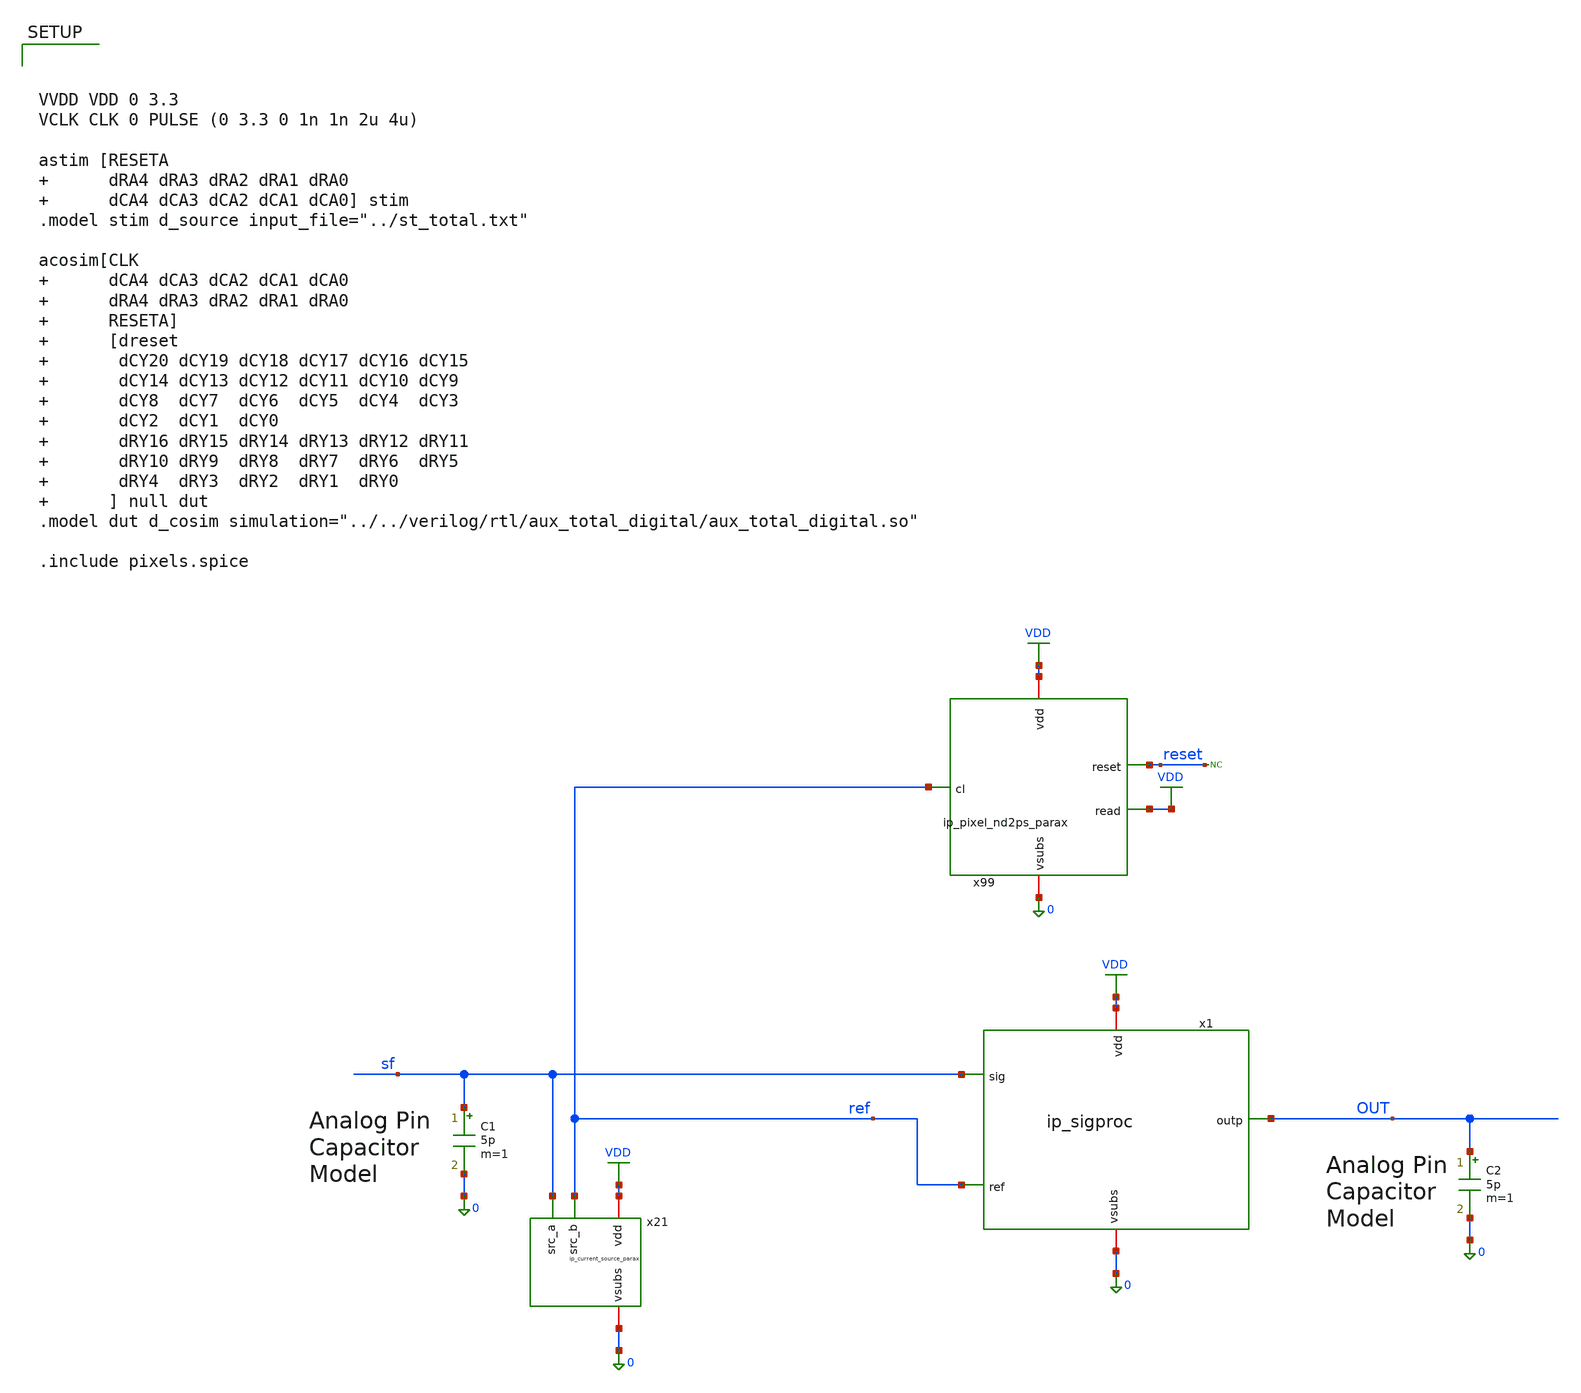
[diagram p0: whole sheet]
** sch_path: xschem/tb_total_tran.sch
**.subckt tb_total_tran
x21 VDD sf 0 ref ip_current_source_parax
x99 VDD reset VDD 0 ref ip_pixel_nd2ps_parax
C1 sf 0 5p m=1
C2 OUT 0 5p m=1
* noconn reset
x1 VDD OUT sf ref 0 ip_sigproc
**** begin user architecture code

.include $::180MCU_MODELS/design.ngspice
.lib $::180MCU_MODELS/sm141064.ngspice typical
.lib $::180MCU_MODELS/sm141064.ngspice res_typical
.lib $::180MCU_MODELS/sm141064.ngspice moscap_typical
.lib $::180MCU_MODELS/sm141064.ngspice diode_typical




.option klu
.option reltol=0.075
.option abstol=200u
.save none

.save V(nRA0) V(nRA1) V(nRA2) V(nRA3) V(nRA4)
.save V(nCA0) V(nCA1) V(nCA2) V(nCA3) V(nCA4)

.save V(ncy0) V(ncy1) V(ncy2) V(ncy3) V(ncy4) V(ncy5) V(ncy6) V(ncy7) V(ncy8)
.save V(ncy9) V(ncy10) V(ncy11) V(ncy12) V(ncy13) V(ncy14) V(ncy15) V(ncy16)
.save V(ncy17) V(ncy18) V(ncy19) V(ncy20)

.save V(nry0) V(nry1) V(nry2) V(nry3) V(nry4) V(nry5) V(nry6) V(nry7) V(nry8)
.save V(nry9) V(nry10) V(nry11) V(nry12) V(nry13) V(nry14) V(nry15) V(nry16)

.save V(reset) V(clk)
.save V(out) V(sf) V(ref) V(amp)
.control
	reset
	tran 1u 9m
	write tb_total_tran.raw
	quit
.endc






VVDD VDD 0 3.3
VCLK CLK 0 PULSE (0 3.3 0 1n 1n 2u 4u)

astim [RESETA        dRA4 dRA3 dRA2 dRA1 dRA0        dCA4 dCA3 dCA2 dCA1 dCA0] stim
.model stim d_source input_file="../st_total.txt"

acosim[CLK        dCA4 dCA3 dCA2 dCA1 dCA0        dRA4 dRA3 dRA2 dRA1 dRA0        RESETA]
+        [dreset        dCY20 dCY19 dCY18 dCY17 dCY16 dCY15        dCY14 dCY13 dCY12 dCY11 dCY10 dCY9         dCY8
+  dCY7  dCY6  dCY5  dCY4  dCY3         dCY2  dCY1  dCY0         dRY16 dRY15 dRY14 dRY13 dRY12 dRY11
+         dRY10 dRY9  dRY8  dRY7  dRY6  dRY5        dRY4  dRY3  dRY2  dRY1  dRY0        ] null dut
.model dut d_cosim simulation="../../verilog/rtl/aux_total_digital/aux_total_digital.so"

.include pixels.spice


**** end user architecture code
**.ends

* expanding   symbol:  ip_current_source_parax.sym # of pins=4
** sym_path: xschem/ip_current_source.sym
.include [file normalize ./parax/ip_current_source.sim.spice]

* expanding   symbol:  ip_pixel_nd2ps_parax.sym # of pins=5
** sym_path: xschem/ip_pixel_nd2ps.sym
.include [file normalize ./parax/ip_pixel_nd2ps.sim.spice]

* expanding   symbol:  ip_sigproc.sym # of pins=5
** sym_path: xschem/ip_sigproc.sym
** sch_path: xschem/ip_sigproc.sch
.subckt ip_sigproc vdd outp sig ref vsubs
*.ipin sig
*.ipin ref
*.iopin vdd
*.iopin vsubs
*.opin outp
x1 vdd net1 sig net1 vsubs ip_amplifier
x2 vdd outp ref net2 net6 ip_amplifier
XR1 net1 net2 net7 ppolyf_u_1k r_width=1e-6 r_length=10e-6 m=1
XR2 net2 net3 net8 ppolyf_u_1k r_width=1e-6 r_length=10e-6 m=1
XR3 net3 net4 net9 ppolyf_u_1k r_width=1e-6 r_length=10e-6 m=1
XR4 net4 net5 net10 ppolyf_u_1k r_width=1e-6 r_length=10e-6 m=1
XR5 net5 outp net11 ppolyf_u_1k r_width=1e-6 r_length=10e-6 m=1
XC1 outp net2 cap_pmos_03v3 c_width=12e-6 c_length=12e-6 m=1
XC2 net2 outp cap_pmos_03v3 c_width=12e-6 c_length=12e-6 m=1
.ends


* expanding   symbol:  xschem/ip_amplifier.sym # of pins=5
** sym_path: xschem/ip_amplifier.sym
** sch_path: xschem/ip_amplifier.sch
.subckt ip_amplifier VDD OUTP INP INN VSUBS
*.iopin VDD
*.iopin VSUBS
*.ipin INP
*.ipin INN
*.opin OUTP
XM1 net10 INP net8 VDD pfet_06v0 L=0.7u W=11.0u nf=1 ad='int((nf+1)/2) * W/nf * 0.18u' as='int((nf+2)/2) * W/nf * 0.18u'
+ pd='2*int((nf+1)/2) * (W/nf + 0.18u)' ps='2*int((nf+2)/2) * (W/nf + 0.18u)' nrd='0.18u / W' nrs='0.18u / W'
+ sa=0 sb=0 sd=0 m=2 par=2
XM2 net9 INN net8 VDD pfet_06v0 L=0.7u W=11.0u nf=1 ad='int((nf+1)/2) * W/nf * 0.18u' as='int((nf+2)/2) * W/nf * 0.18u'
+ pd='2*int((nf+1)/2) * (W/nf + 0.18u)' ps='2*int((nf+2)/2) * (W/nf + 0.18u)' nrd='0.18u / W' nrs='0.18u / W'
+ sa=0 sb=0 sd=0 m=2 par=2
XM5 net10 net1 VSUBS vsubs nfet_06v0 L=2u W=5u nf=1 ad='int((nf+1)/2) * W/nf * 0.18u' as='int((nf+2)/2) * W/nf * 0.18u'
+ pd='2*int((nf+1)/2) * (W/nf + 0.18u)' ps='2*int((nf+2)/2) * (W/nf + 0.18u)' nrd='0.18u / W' nrs='0.18u / W'
+ sa=0 sb=0 sd=0 m=1 par=1
XM6 net9 net1 VSUBS vsubs nfet_06v0 L=2u W=5u nf=1 ad='int((nf+1)/2) * W/nf * 0.18u' as='int((nf+2)/2) * W/nf * 0.18u'
+ pd='2*int((nf+1)/2) * (W/nf + 0.18u)' ps='2*int((nf+2)/2) * (W/nf + 0.18u)' nrd='0.18u / W' nrs='0.18u / W'
+ sa=0 sb=0 sd=0 m=1 par=1
XM3 net3 net1 VSUBS vsubs nfet_06v0 L=1u W=12.5u nf=1 ad='int((nf+1)/2) * W/nf * 0.18u' as='int((nf+2)/2) * W/nf * 0.18u'
+ pd='2*int((nf+1)/2) * (W/nf + 0.18u)' ps='2*int((nf+2)/2) * (W/nf + 0.18u)' nrd='0.18u / W' nrs='0.18u / W'
+ sa=0 sb=0 sd=0 m=2 par=2
XM4 net2 net1 VSUBS vsubs nfet_06v0 L=1u W=5u nf=1 ad='int((nf+1)/2) * W/nf * 0.18u' as='int((nf+2)/2) * W/nf * 0.18u'
+ pd='2*int((nf+1)/2) * (W/nf + 0.18u)' ps='2*int((nf+2)/2) * (W/nf + 0.18u)' nrd='0.18u / W' nrs='0.18u / W'
+ sa=0 sb=0 sd=0 m=1 par=1
XM7 net1 net1 net3 vsubs nfet_06v0 L=0.7u W=14u nf=1 ad='int((nf+1)/2) * W/nf * 0.18u' as='int((nf+2)/2) * W/nf * 0.18u'
+ pd='2*int((nf+1)/2) * (W/nf + 0.18u)' ps='2*int((nf+2)/2) * (W/nf + 0.18u)' nrd='0.18u / W' nrs='0.18u / W'
+ sa=0 sb=0 sd=0 m=2 par=2
XM8 net4 net1 net2 vsubs nfet_06v0 L=0.7u W=14u nf=1 ad='int((nf+1)/2) * W/nf * 0.18u' as='int((nf+2)/2) * W/nf * 0.18u'
+ pd='2*int((nf+1)/2) * (W/nf + 0.18u)' ps='2*int((nf+2)/2) * (W/nf + 0.18u)' nrd='0.18u / W' nrs='0.18u / W'
+ sa=0 sb=0 sd=0 m=2 par=2
XM9 net5 net7 VDD VDD pfet_06v0 L=1u W=6u nf=1 ad='int((nf+1)/2) * W/nf * 0.18u' as='int((nf+2)/2) * W/nf * 0.18u'
+ pd='2*int((nf+1)/2) * (W/nf + 0.18u)' ps='2*int((nf+2)/2) * (W/nf + 0.18u)' nrd='0.18u / W' nrs='0.18u / W'
+ sa=0 sb=0 sd=0 m=1 par=1
XM10 net6 net7 VDD VDD pfet_06v0 L=1u W=6u nf=1 ad='int((nf+1)/2) * W/nf * 0.18u' as='int((nf+2)/2) * W/nf * 0.18u'
+ pd='2*int((nf+1)/2) * (W/nf + 0.18u)' ps='2*int((nf+2)/2) * (W/nf + 0.18u)' nrd='0.18u / W' nrs='0.18u / W'
+ sa=0 sb=0 sd=0 m=1 par=1
XM11 net7 net7 net5 VDD pfet_06v0 L=0.7u W=14u nf=1 ad='int((nf+1)/2) * W/nf * 0.18u' as='int((nf+2)/2) * W/nf * 0.18u'
+ pd='2*int((nf+1)/2) * (W/nf + 0.18u)' ps='2*int((nf+2)/2) * (W/nf + 0.18u)' nrd='0.18u / W' nrs='0.18u / W'
+ sa=0 sb=0 sd=0 m=2 par=2
XM12 net8 net7 net6 VDD pfet_06v0 L=0.7u W=14u nf=1 ad='int((nf+1)/2) * W/nf * 0.18u' as='int((nf+2)/2) * W/nf * 0.18u'
+ pd='2*int((nf+1)/2) * (W/nf + 0.18u)' ps='2*int((nf+2)/2) * (W/nf + 0.18u)' nrd='0.18u / W' nrs='0.18u / W'
+ sa=0 sb=0 sd=0 m=2 par=2
XM13 net11 net1 net9 vsubs nfet_06v0 L=0.7u W=12u nf=1 ad='int((nf+1)/2) * W/nf * 0.18u' as='int((nf+2)/2) * W/nf * 0.18u'
+ pd='2*int((nf+1)/2) * (W/nf + 0.18u)' ps='2*int((nf+2)/2) * (W/nf + 0.18u)' nrd='0.18u / W' nrs='0.18u / W'
+ sa=0 sb=0 sd=0 m=1 par=1
XM14 COMP net1 net10 vsubs nfet_06v0 L=0.7u W=12u nf=1 ad='int((nf+1)/2) * W/nf * 0.18u' as='int((nf+2)/2) * W/nf * 0.18u'
+ pd='2*int((nf+1)/2) * (W/nf + 0.18u)' ps='2*int((nf+2)/2) * (W/nf + 0.18u)' nrd='0.18u / W' nrs='0.18u / W'
+ sa=0 sb=0 sd=0 m=1 par=1
XM15 net11 net11 VDD VDD pfet_06v0 L=0.7u W=12u nf=1 ad='int((nf+1)/2) * W/nf * 0.18u' as='int((nf+2)/2) * W/nf * 0.18u'
+ pd='2*int((nf+1)/2) * (W/nf + 0.18u)' ps='2*int((nf+2)/2) * (W/nf + 0.18u)' nrd='0.18u / W' nrs='0.18u / W'
+ sa=0 sb=0 sd=0 m=1 par=1
XM16 COMP net11 VDD VDD pfet_06v0 L=0.7u W=12u nf=1 ad='int((nf+1)/2) * W/nf * 0.18u' as='int((nf+2)/2) * W/nf * 0.18u'
+ pd='2*int((nf+1)/2) * (W/nf + 0.18u)' ps='2*int((nf+2)/2) * (W/nf + 0.18u)' nrd='0.18u / W' nrs='0.18u / W'
+ sa=0 sb=0 sd=0 m=1 par=1
XM17 OUTP COMP VDD VDD pfet_06v0 L=0.7u W=12u nf=1 ad='int((nf+1)/2) * W/nf * 0.18u' as='int((nf+2)/2) * W/nf * 0.18u'
+ pd='2*int((nf+1)/2) * (W/nf + 0.18u)' ps='2*int((nf+2)/2) * (W/nf + 0.18u)' nrd='0.18u / W' nrs='0.18u / W'
+ sa=0 sb=0 sd=0 m=5 par=5
XM18 OUTP net10 VSUBS vsubs nfet_06v0 L=0.7u W=12u nf=1 ad='int((nf+1)/2) * W/nf * 0.18u' as='int((nf+2)/2) * W/nf * 0.18u'
+ pd='2*int((nf+1)/2) * (W/nf + 0.18u)' ps='2*int((nf+2)/2) * (W/nf + 0.18u)' nrd='0.18u / W' nrs='0.18u / W'
+ sa=0 sb=0 sd=0 m=3 par=3
XR3 net1 net14 vsubs ppolyf_u_1k_6p0 r_width=1e-6 r_length=6e-6 m=1
XR6 net14 net13 vsubs ppolyf_u_1k_6p0 r_width=1e-6 r_length=6e-6 m=1
XR7 net13 net12 vsubs ppolyf_u_1k_6p0 r_width=1e-6 r_length=6e-6 m=1
XR8 net12 net15 vsubs ppolyf_u_1k_6p0 r_width=1e-6 r_length=4e-6 m=1
Vmeas VDD net15 0
Vmeas1 net7 net4 0
XC1 OUTP net16 cap_nmos_03v3 c_width=12e-6 c_length=18e-6 m=1
XC2 COMP net17 cap_nmos_03v3 c_width=12e-6 c_length=18e-6 m=1
XR12 net16 COMP vsubs ppolyf_u_1k_6p0 r_width=1e-6 r_length=10e-6 m=1
XR16 OUTP net17 vsubs ppolyf_u_1k_6p0 r_width=1e-6 r_length=10e-6 m=1
.ends

.GLOBAL VDD
.end
